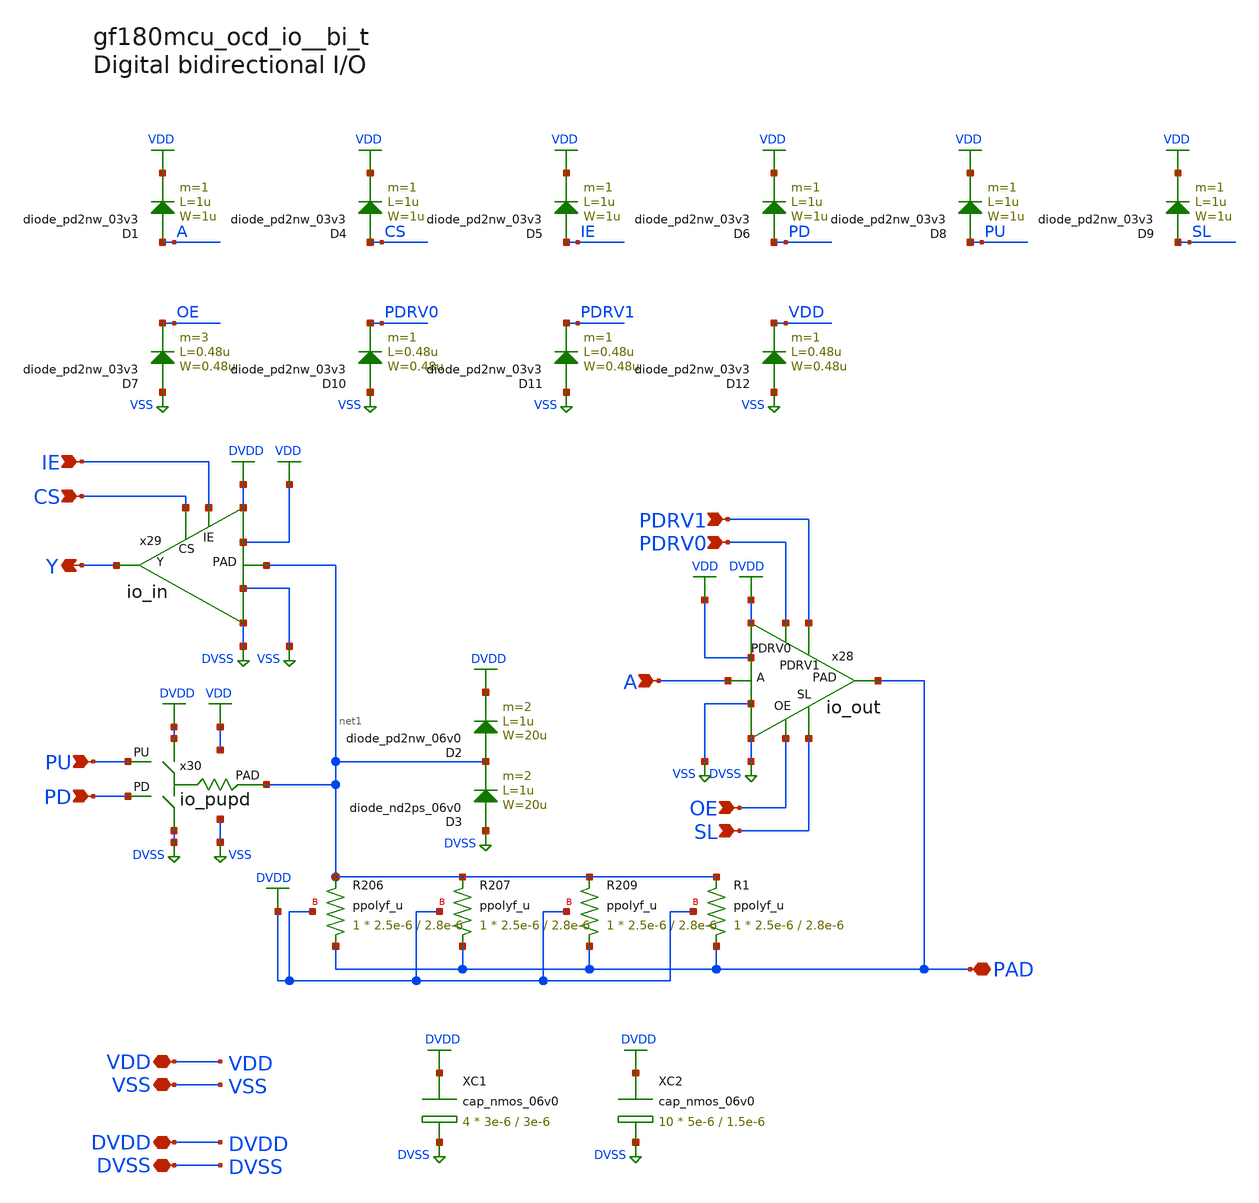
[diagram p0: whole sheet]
** sch_path: cells/bi_t/gf180mcu_ocd_io__bi_t.sch
* Copyright 2023 David Mitchell Bailey
* Licensed under the Apache License, Version 2.0 (the "License");
* you may not use this file except in compliance with the License.
* You may obtain a copy of the License at
* https://www.apache.org/licenses/LICENSE-2.0
* Unless required by applicable law or agreed to in writing, software
* distributed under the License is distributed on an "AS IS" BASIS,
* WITHOUT WARRANTIES OR CONDITIONS OF ANY KIND, either express or implied.
* See the License for the specific language governing permissions and
* limitations under the License.
**.subckt gf180mcu_ocd_io__bi_t A VDD Y VSS DVDD DVSS PU PD PDRV0 PDRV1 SL OE CS IE PAD
*.ipin A
*.iopin VDD
*.opin Y
*.iopin VSS
*.iopin DVDD
*.iopin DVSS
*.ipin PU
*.ipin PD
*.ipin PDRV0
*.ipin PDRV1
*.ipin SL
*.ipin OE
*.ipin CS
*.ipin IE
*.iopin PAD
XR206 PAD net1 DVDD ppolyf_u r_width=2.5e-6 r_length=2.8e-6 m=1
XR207 PAD net1 DVDD ppolyf_u r_width=2.5e-6 r_length=2.8e-6 m=1
XR209 PAD net1 DVDD ppolyf_u r_width=2.5e-6 r_length=2.8e-6 m=1
XR1 PAD net1 DVDD ppolyf_u r_width=2.5e-6 r_length=2.8e-6 m=1
x28 OE A SL PDRV0 PDRV1 PAD DVDD DVSS VDD VSS io_out
x29 net1 IE CS Y DVDD DVSS VDD VSS io_in
x30 DVDD DVSS PU PD net1 VDD VSS io_pupd
XC1 DVDD DVSS cap_nmos_06v0 c_width=3e-6 c_length=3e-6 m=4
XC2 DVDD DVSS cap_nmos_06v0 c_width=5e-6 c_length=1.5e-6 m=10
D3 DVSS net1 diode_nd2ps_06v0 area='20u * 1u ' pj='2*20u + 2*1u ' m=2
D2 net1 DVDD diode_pd2nw_06v0 area='20u * 1u ' pj='2*20u + 2*1u ' m=2
D1 A VDD diode_pd2nw_03v3 area='1u * 1u ' pj='2*1u + 2*1u ' m=1
D7 VSS OE diode_pd2nw_03v3 area='0.48u * 0.48u ' pj='2*0.48u + 2*0.48u ' m=3
D4 CS VDD diode_pd2nw_03v3 area='1u * 1u ' pj='2*1u + 2*1u ' m=1
D5 IE VDD diode_pd2nw_03v3 area='1u * 1u ' pj='2*1u + 2*1u ' m=1
D6 PD VDD diode_pd2nw_03v3 area='1u * 1u ' pj='2*1u + 2*1u ' m=1
D8 PU VDD diode_pd2nw_03v3 area='1u * 1u ' pj='2*1u + 2*1u ' m=1
D9 SL VDD diode_pd2nw_03v3 area='1u * 1u ' pj='2*1u + 2*1u ' m=1
D10 VSS PDRV0 diode_pd2nw_03v3 area='0.48u * 0.48u ' pj='2*0.48u + 2*0.48u ' m=1
D11 VSS PDRV1 diode_pd2nw_03v3 area='0.48u * 0.48u ' pj='2*0.48u + 2*0.48u ' m=1
D12 VSS VDD diode_pd2nw_03v3 area='0.48u * 0.48u ' pj='2*0.48u + 2*0.48u ' m=1
**.ends
.GLOBAL DVSS
.GLOBAL DVDD
.GLOBAL VDD
.GLOBAL VSS
.end
